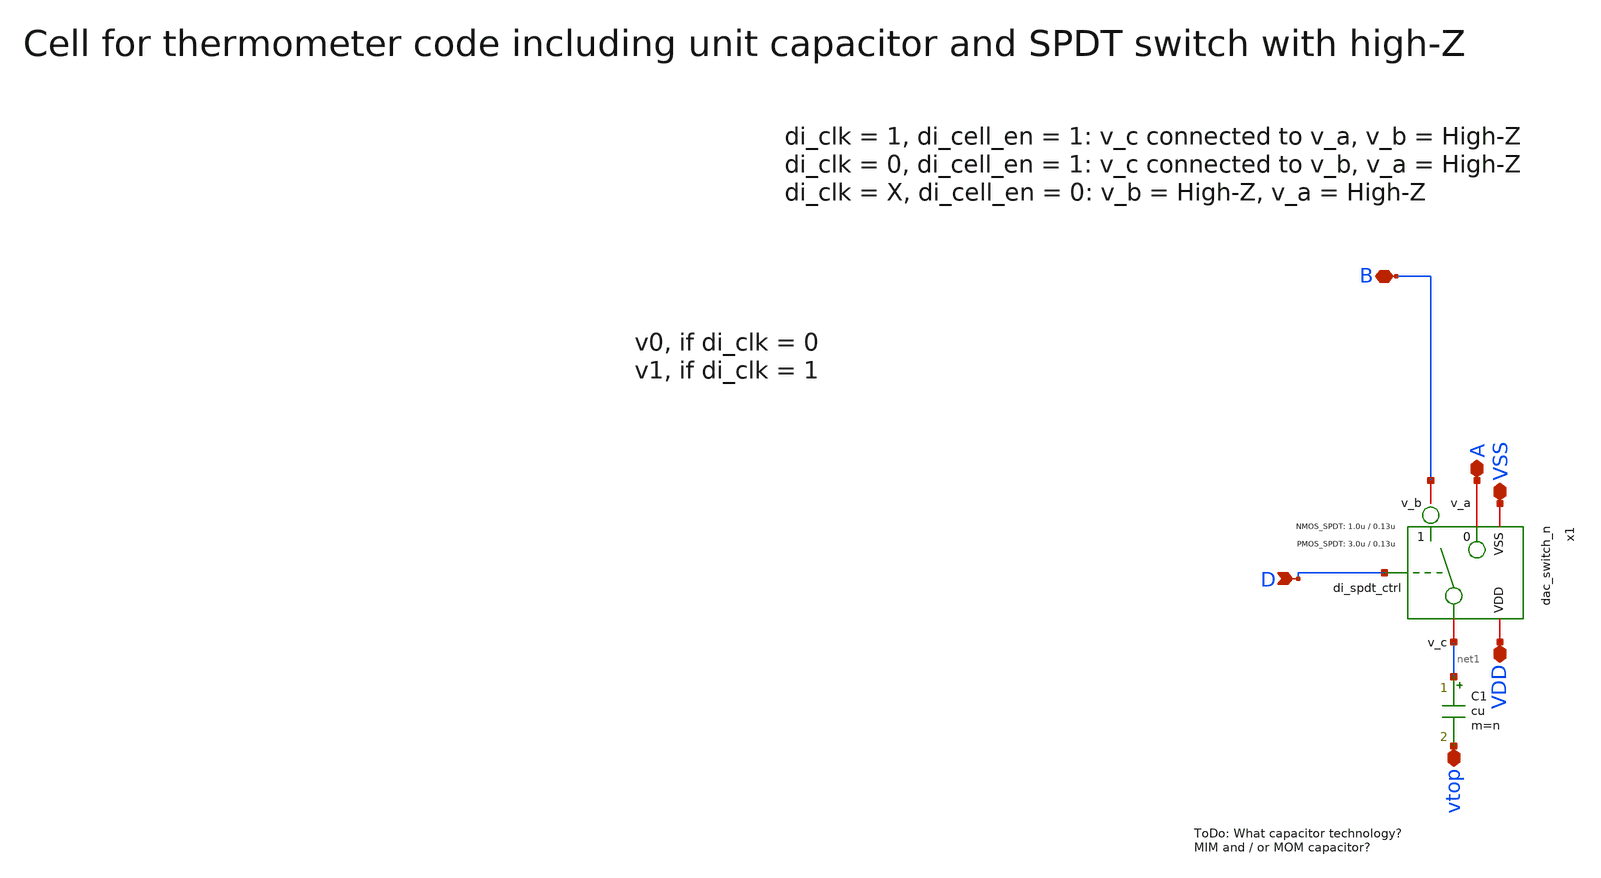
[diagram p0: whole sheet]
** sch_path: xschem/dac_icms_cell/unit_cell_n.sch
**.subckt unit_cell_n VSS A VDD D B vtop
*.iopin VSS
*.iopin A
*.iopin VDD
*.ipin D
*.iopin B
*.iopin vtop
x1 VDD D VSS net1 B A dac_switch_n W_P_TG=3.0u L_P_TG=0.13u W_N_TG=1.0u L_N_TG=0.13u n=n
C1 net1 vtop cu m=n
**.ends

* expanding   symbol:  dac_icms_cell/dac_switch_n.sym # of pins=6
** sym_path: xschem/dac_icms_cell/dac_switch_n.sym
** sch_path: xschem/dac_icms_cell/dac_switch_n.sch
.subckt dac_switch_n VDD di_spdt_ctrl VSS v_c v_b v_a  W_P_TG=3.0u L_P_TG=0.13u W_N_TG=1.0u
+ L_N_TG=0.13u n=1
*.iopin v_a
*.iopin v_c
*.iopin VDD
*.iopin VSS
*.ipin di_spdt_ctrl
*.iopin v_b
x1 VDD di_spdt_ctrl_n VSS v_c v_a di_spdt_ctrl transmission_gate_lv_wo_dummy W_P=W_P_TG L_P=L_P_TG
+ W_N=W_N_TG L_N=L_N_TG W_P_D=1.0u L_P_D=0.13u W_N_D=1.0u L_N_D=0.13u n=n
x8 VDD di_spdt_ctrl di_spdt_ctrl_n VSS inverter_lv W_P=W_P_TG L_P=L_P_TG W_N=W_N_TG L_N=L_N_TG N_C=1
XM1 net1 net2 VSS VSS sg13_lv_nmos w=0.5u l=0.2u ng=1 m=n mm_ok=1
XM3 net1 net2 VDD VDD sg13_lv_pmos w=1u l=0.2u ng=1 m=n mm_ok=1
x2 VDD di_spdt_ctrl VSS v_c net1 di_spdt_ctrl_n transmission_gate_lv_w_dummy W_P=W_P_TG L_P=L_P_TG
+ W_N=W_N_TG L_N=L_N_TG W_P_D=1.0u L_P_D=0.13u W_N_D=1.0u L_N_D=0.13u n=n
XM2 net2 v_b VSS VSS sg13_lv_nmos w=0.5u l=0.2u ng=1 m=10 mm_ok=1
XM4 net2 v_b VDD VDD sg13_lv_pmos w=1u l=0.2u ng=1 m=10 mm_ok=1
.ends


* expanding   symbol:  transmission_gate/transmission_gate_lv_wo_dummy.sym # of pins=6
** sym_path: xschem/transmission_gate/transmission_gate_lv_wo_dummy.sym
** sch_path: xschem/transmission_gate/transmission_gate_lv_wo_dummy.sch
.subckt transmission_gate_lv_wo_dummy VDD di_tg_ctrl VSS v_b v_a di_tg_ctrl_n  W_P=2.0u L_P=0.13u
+ W_N=2.0u L_N=0.13u W_P_D=1.0u L_P_D=0.13u W_N_D=1.0u L_N_D=0.13u n=1
*.iopin v_a
*.iopin v_b
*.iopin VDD
*.iopin VSS
*.ipin di_tg_ctrl
*.ipin di_tg_ctrl_n
XM1 v_a di_tg_ctrl v_b VSS sg13_lv_nmos w=W_N l=L_N ng=1 m=n mm_ok=1
XM2 v_a di_tg_ctrl_n v_b VDD sg13_lv_pmos w=W_P l=L_P ng=1 m=n mm_ok=1
.ends


* expanding   symbol:  inverter/inverter_lv.sym # of pins=4
** sym_path: xschem/inverter/inverter_lv.sym
** sch_path: xschem/inverter/inverter_lv.sch
.subckt inverter_lv VDD vin vout VSS  W_P=3.0u L_P=0.13u W_N=1.0u L_N=0.13u N_C=1
*.ipin vin
*.iopin VDD
*.iopin VSS
*.opin vout
XM1 vout vin VDD VDD sg13_lv_pmos w=W_P l=L_P ng=1 m={N_C} mm_ok=1
XM2 vout vin VSS VSS sg13_lv_nmos w=W_N l=L_N ng=1 m={N_C} mm_ok=1
.ends


* expanding   symbol:  transmission_gate/transmission_gate_lv_w_dummy.sym # of pins=6
** sym_path: xschem/transmission_gate/transmission_gate_lv_w_dummy.sym
** sch_path: xschem/transmission_gate/transmission_gate_lv_w_dummy.sch
.subckt transmission_gate_lv_w_dummy VDD di_tg_ctrl VSS v_b v_a di_tg_ctrl_n  W_P=2.0u L_P=0.13u
+ W_N=2.0u L_N=0.13u W_P_D=1.0u L_P_D=0.13u W_N_D=1.0u L_N_D=0.13u n=1
*.iopin v_a
*.iopin v_b
*.iopin VDD
*.iopin VSS
*.ipin di_tg_ctrl
*.ipin di_tg_ctrl_n
XM1 v_a di_tg_ctrl v_b VSS sg13_lv_nmos w=W_N l=L_N ng=1 m=n mm_ok=1
XM2 v_a di_tg_ctrl_n v_b VDD sg13_lv_pmos w=W_P l=L_P ng=1 m=n mm_ok=1
XMdummy2 v_b di_tg_ctrl v_b VDD sg13_lv_pmos w=W_P l=L_P ng=1 m={n/2} mm_ok=1
XMdummy1 v_b di_tg_ctrl_n v_b VSS sg13_lv_nmos w=W_N l=L_N ng=1 m={n/2} mm_ok=1
.ends

.end
